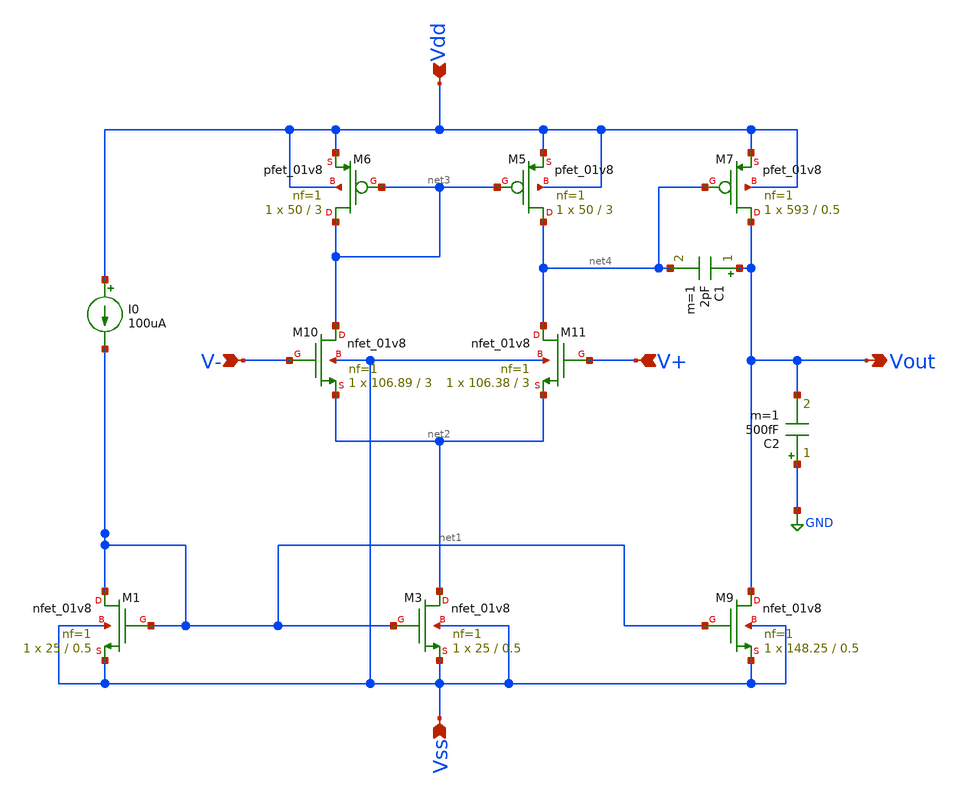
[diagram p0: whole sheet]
** sch_path: xschem/op_amp_3.sch
**.subckt op_amp_3 Vout Vdd Vss V+ V-
*.opin Vout
*.ipin Vdd
*.ipin Vss
*.ipin V+
*.ipin V-
XM1 net1 net1 Vss Vss sky130_fd_pr__nfet_01v8 L=0.5 W=25 nf=1 ad='int((1 + 1)/2) * 25 / 1 * 0.29' as='int((1 + 2)/2) * 25 / 1 * 0.29'
+ pd='2*int((1 + 1)/2) * (25 / 1 + 0.29)' ps='2*int((1 + 2)/2) * (25 / 1 + 0.29)' nrd='0.29 / 25 ' nrs='0.29 / 25 '
+ sa=0 sb=0 sd=0 mult=1 m=1
XM3 net2 net1 Vss Vss sky130_fd_pr__nfet_01v8 L=0.5 W=25 nf=1 ad='int((1 + 1)/2) * 25 / 1 * 0.29' as='int((1 + 2)/2) * 25 / 1 * 0.29'
+ pd='2*int((1 + 1)/2) * (25 / 1 + 0.29)' ps='2*int((1 + 2)/2) * (25 / 1 + 0.29)' nrd='0.29 / 25 ' nrs='0.29 / 25 '
+ sa=0 sb=0 sd=0 mult=1 m=1
XM10 net3 V- net2 Vss sky130_fd_pr__nfet_01v8 L=3 W=106.89 nf=1 ad='int((1 + 1)/2) * 106.89 / 1 * 0.29'
+ as='int((1 + 2)/2) * 106.89 / 1 * 0.29' pd='2*int((1 + 1)/2) * (106.89 / 1 + 0.29)' ps='2*int((1 + 2)/2) * (106.89 / 1 + 0.29)'
+ nrd='0.29 / 106.89 ' nrs='0.29 / 106.89 ' sa=0 sb=0 sd=0 mult=1 m=1
XM11 net4 V+ net2 Vss sky130_fd_pr__nfet_01v8 L=3 W=106.38 nf=1 ad='int((1 + 1)/2) * 106.38 / 1 * 0.29'
+ as='int((1 + 2)/2) * 106.38 / 1 * 0.29' pd='2*int((1 + 1)/2) * (106.38 / 1 + 0.29)' ps='2*int((1 + 2)/2) * (106.38 / 1 + 0.29)'
+ nrd='0.29 / 106.38 ' nrs='0.29 / 106.38 ' sa=0 sb=0 sd=0 mult=1 m=1
XM5 net4 net3 Vdd Vdd sky130_fd_pr__pfet_01v8 L=3 W=50 nf=1 ad='int((1 + 1)/2) * 50 / 1 * 0.29' as='int((1 + 2)/2) * 50 / 1 * 0.29'
+ pd='2*int((1 + 1)/2) * (50 / 1 + 0.29)' ps='2*int((1 + 2)/2) * (50 / 1 + 0.29)' nrd='0.29 / 50 ' nrs='0.29 / 50 '
+ sa=0 sb=0 sd=0 mult=1 m=1
XM6 net3 net3 Vdd Vdd sky130_fd_pr__pfet_01v8 L=3 W=50 nf=1 ad='int((1 + 1)/2) * 50 / 1 * 0.29' as='int((1 + 2)/2) * 50 / 1 * 0.29'
+ pd='2*int((1 + 1)/2) * (50 / 1 + 0.29)' ps='2*int((1 + 2)/2) * (50 / 1 + 0.29)' nrd='0.29 / 50 ' nrs='0.29 / 50 '
+ sa=0 sb=0 sd=0 mult=1 m=1
C1 Vout net4 2pF m=1
C2 GND Vout 500fF m=1
XM7 Vout net4 Vdd Vdd sky130_fd_pr__pfet_01v8 L=0.5 W=593 nf=1 ad='int((1 + 1)/2) * 593 / 1 * 0.29' as='int((1 + 2)/2) * 593 / 1 * 0.29'
+ pd='2*int((1 + 1)/2) * (593 / 1 + 0.29)' ps='2*int((1 + 2)/2) * (593 / 1 + 0.29)' nrd='0.29 / 593 ' nrs='0.29 / 593 '
+ sa=0 sb=0 sd=0 mult=1 m=1
XM9 Vout net1 Vss Vss sky130_fd_pr__nfet_01v8 L=0.5 W=148.25 nf=1 ad='int((1 + 1)/2) * 148.25 / 1 * 0.29'
+ as='int((1 + 2)/2) * 148.25 / 1 * 0.29' pd='2*int((1 + 1)/2) * (148.25 / 1 + 0.29)' ps='2*int((1 + 2)/2) * (148.25 / 1 + 0.29)'
+ nrd='0.29 / 148.25 ' nrs='0.29 / 148.25 ' sa=0 sb=0 sd=0 mult=1 m=1
I0 Vdd net1 100uA
**.ends
.GLOBAL GND
.end
